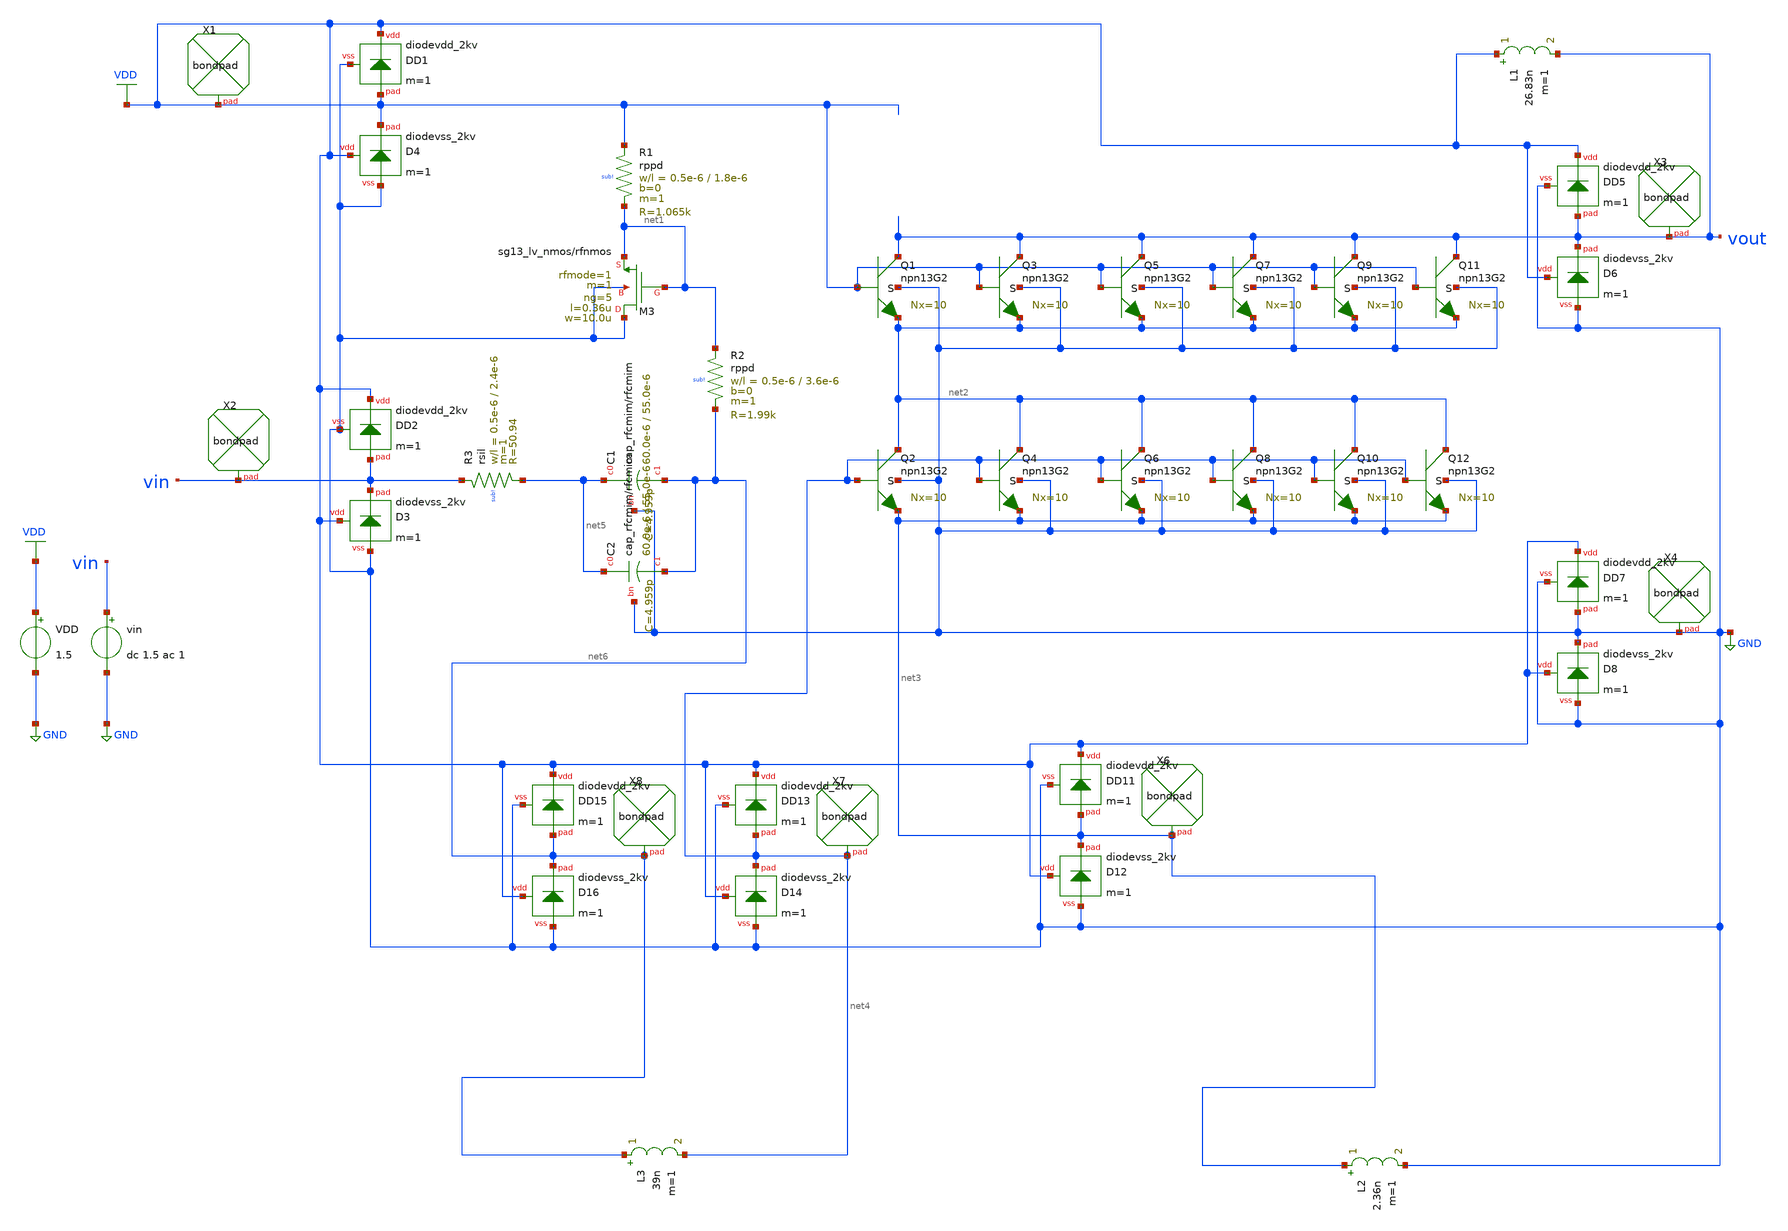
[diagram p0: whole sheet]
** sch_path: GPS_LNA/design_data/xyce/lna_tb_xyce_rf_npn_pad.sch
**.subckt lna_tb_xyce_rf_npn_pad
VDD VDD GND 1.5
vin vin GND dc 1.5 ac 1
XR2 net1 net6 sub! rppd w=0.5e-6 l=3.6e-6 m=1 b=0 mm_ok=1
XR1 VDD net1 sub! rppd w=0.5e-6 l=1.8e-6 m=1 b=0 mm_ok=1
XR3 vin net5 sub! rsil w=0.5e-6 l=2.4e-6 m=1 mm_ok=1
L1 VDD vout 26.83n m=1
L2 net3 GND 2.36n m=1
L3 net6 net4 39n m=1
XC1 net5 net6 GND cap_rfcmim w=60.0e-6 l=55.0e-6 wfeed=5.0e-6 m=1 mm_ok=1
XC2 net5 net6 GND cap_rfcmim w=60.0e-6 l=55.0e-6 wfeed=5.0e-6 m=1 mm_ok=1
XM3 GND net1 net1 GND sg13_lv_nmos w=10.0u l=0.36u ng=5 m=1 rfmode=1 mm_ok=1
XX1 VDD bondpad size=100u shape=0 padtype=0
XX3 vout bondpad size=100u shape=0 padtype=0
XX4 GND bondpad size=100u shape=0 padtype=0
XD1 VDD VDD GND diodevdd_2kv m=1
XD4 VDD VDD GND diodevss_2kv m=1
XX2 vin bondpad size=100u shape=0 padtype=0
XQ1 vout VDD net2 GND npn13G2 Nx=10 mm_ok=1
XQ2 net2 net4 net3 GND npn13G2 Nx=10 mm_ok=1
XQ3 vout VDD net2 GND npn13G2 Nx=10 mm_ok=1
XQ4 net2 net4 net3 GND npn13G2 Nx=10 mm_ok=1
XQ5 vout VDD net2 GND npn13G2 Nx=10 mm_ok=1
XQ6 net2 net4 net3 GND npn13G2 Nx=10 mm_ok=1
XQ7 vout VDD net2 GND npn13G2 Nx=10 mm_ok=1
XQ8 net2 net4 net3 GND npn13G2 Nx=10 mm_ok=1
XD2 VDD vin GND diodevdd_2kv m=1
XD3 VDD vin GND diodevss_2kv m=1
XD5 VDD vout GND diodevdd_2kv m=1
XD6 VDD vout GND diodevss_2kv m=1
XD7 VDD GND GND diodevdd_2kv m=1
XD8 VDD GND GND diodevss_2kv m=1
XQ9 vout VDD net2 GND npn13G2 Nx=10 mm_ok=1
XQ10 net2 net4 net3 GND npn13G2 Nx=10 mm_ok=1
XQ11 vout VDD net2 GND npn13G2 Nx=10 mm_ok=1
XQ12 net2 net4 net3 GND npn13G2 Nx=10 mm_ok=1
XX6 net3 bondpad size=100u shape=0 padtype=0
XD11 VDD net3 GND diodevdd_2kv m=1
XD12 VDD net3 GND diodevss_2kv m=1
XX7 net4 bondpad size=100u shape=0 padtype=0
XD13 VDD net4 GND diodevdd_2kv m=1
XD14 VDD net4 GND diodevss_2kv m=1
XX8 net6 bondpad size=100u shape=0 padtype=0
XD15 VDD net6 GND diodevdd_2kv m=1
XD16 VDD net6 GND diodevss_2kv m=1
**** begin user architecture code

.lib $::SG13G2_MODELS_XYCE/cornerHBT.lib hbt_typ
.lib $::SG13G2_MODELS_XYCE/cornerMOSlv.lib mos_tt
.lib $::SG13G2_MODELS_XYCE/resistors.lib res_typ
.lib $::SG13G2_MODELS_XYCE/cornerCAP.lib cap_typ
.include $::SG13G2_MODELS_XYCE/sg13g2_bondpad.lib
.include $::SG13G2_MODELS_XYCE/sg13g2_esd.lib



*.control
.OPTIONS OUTPUT PRINTHEADER=false PRINTFOOTER=false
.preprocess replaceground true
.option temp=27

.ac dec 1001 800meg 3000meg
.print ac format=raw file=lna_tb_xyce_rf_npn_pad.raw V(Vout)


**** end user architecture code
**.ends
.GLOBAL GND
.GLOBAL VDD
.end
